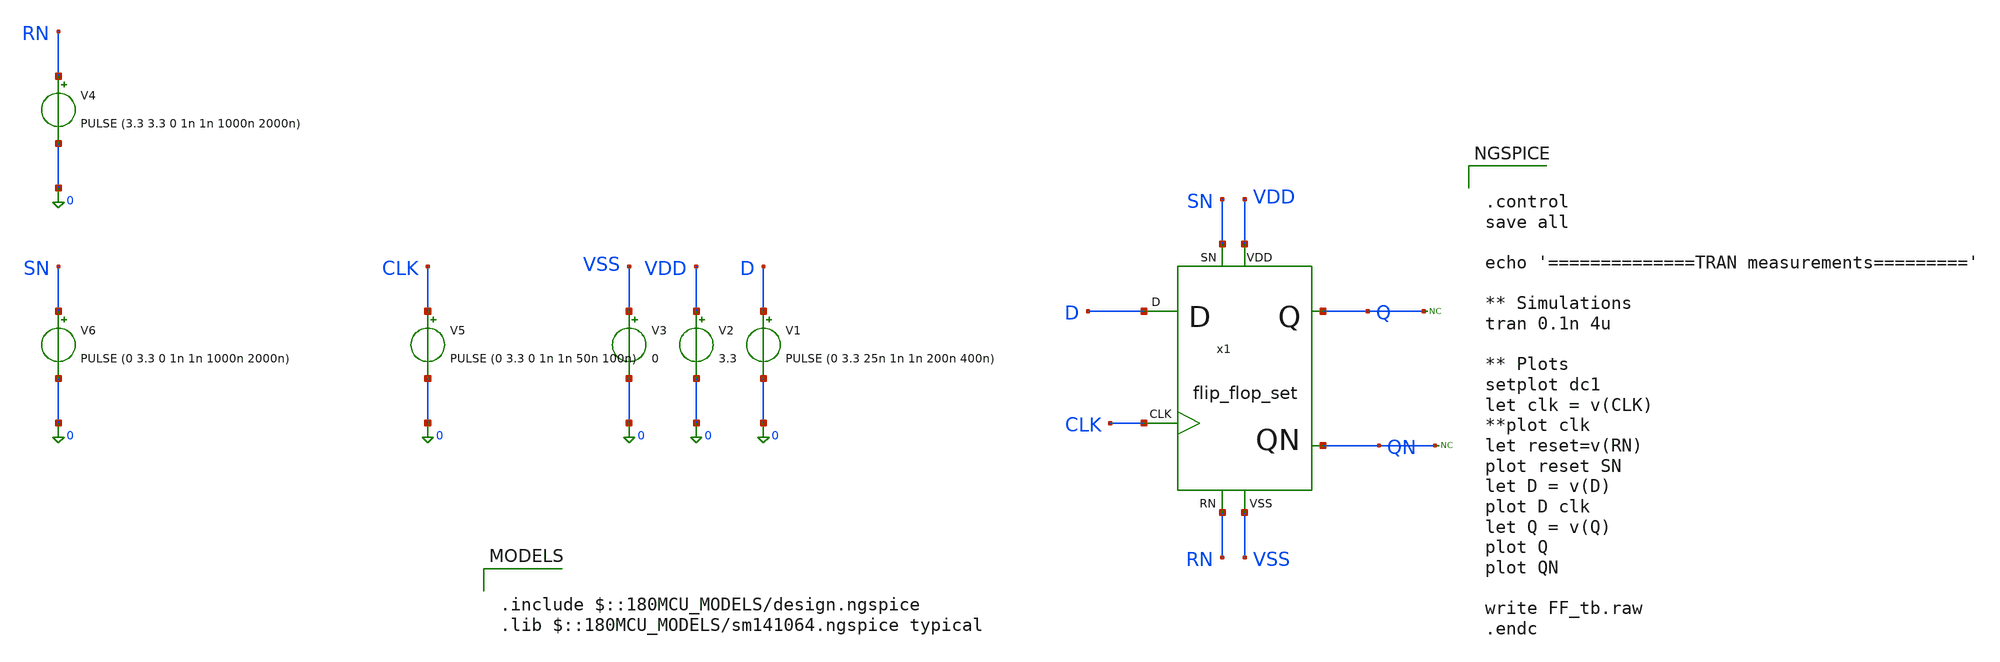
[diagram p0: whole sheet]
** sch_path: designs/sar_adc/digital/flip_flop_set/xschem/flip_flop_set_tb.sch
**.subckt flip_flop_set_tb
V1 D 0 PULSE (0 3.3 25n 1n 1n 200n 400n)
V2 VDD 0 3.3
V3 VSS 0 0
V5 CLK 0 PULSE (0 3.3 0 1n 1n 50n 100n)
V4 RN 0 PULSE (3.3 3.3 0 1n 1n 1000n 2000n)
* noconn Q
* noconn QN
V6 SN 0 PULSE (0 3.3 0 1n 1n 1000n 2000n)
x1 CLK D VDD VSS Q RN QN SN flip_flop_set
**** begin user architecture code

.include $::180MCU_MODELS/design.ngspice
.lib $::180MCU_MODELS/sm141064.ngspice typical



.control
save all

echo '==============TRAN measurements========='

** Simulations
tran 0.1n 4u

** Plots
setplot dc1
let clk = v(CLK)
**plot clk
let reset=v(RN)
plot reset SN
let D = v(D)
plot D clk
let Q = v(Q)
plot Q
plot QN

write FF_tb.raw
.endc


**** end user architecture code
**.ends
.end
